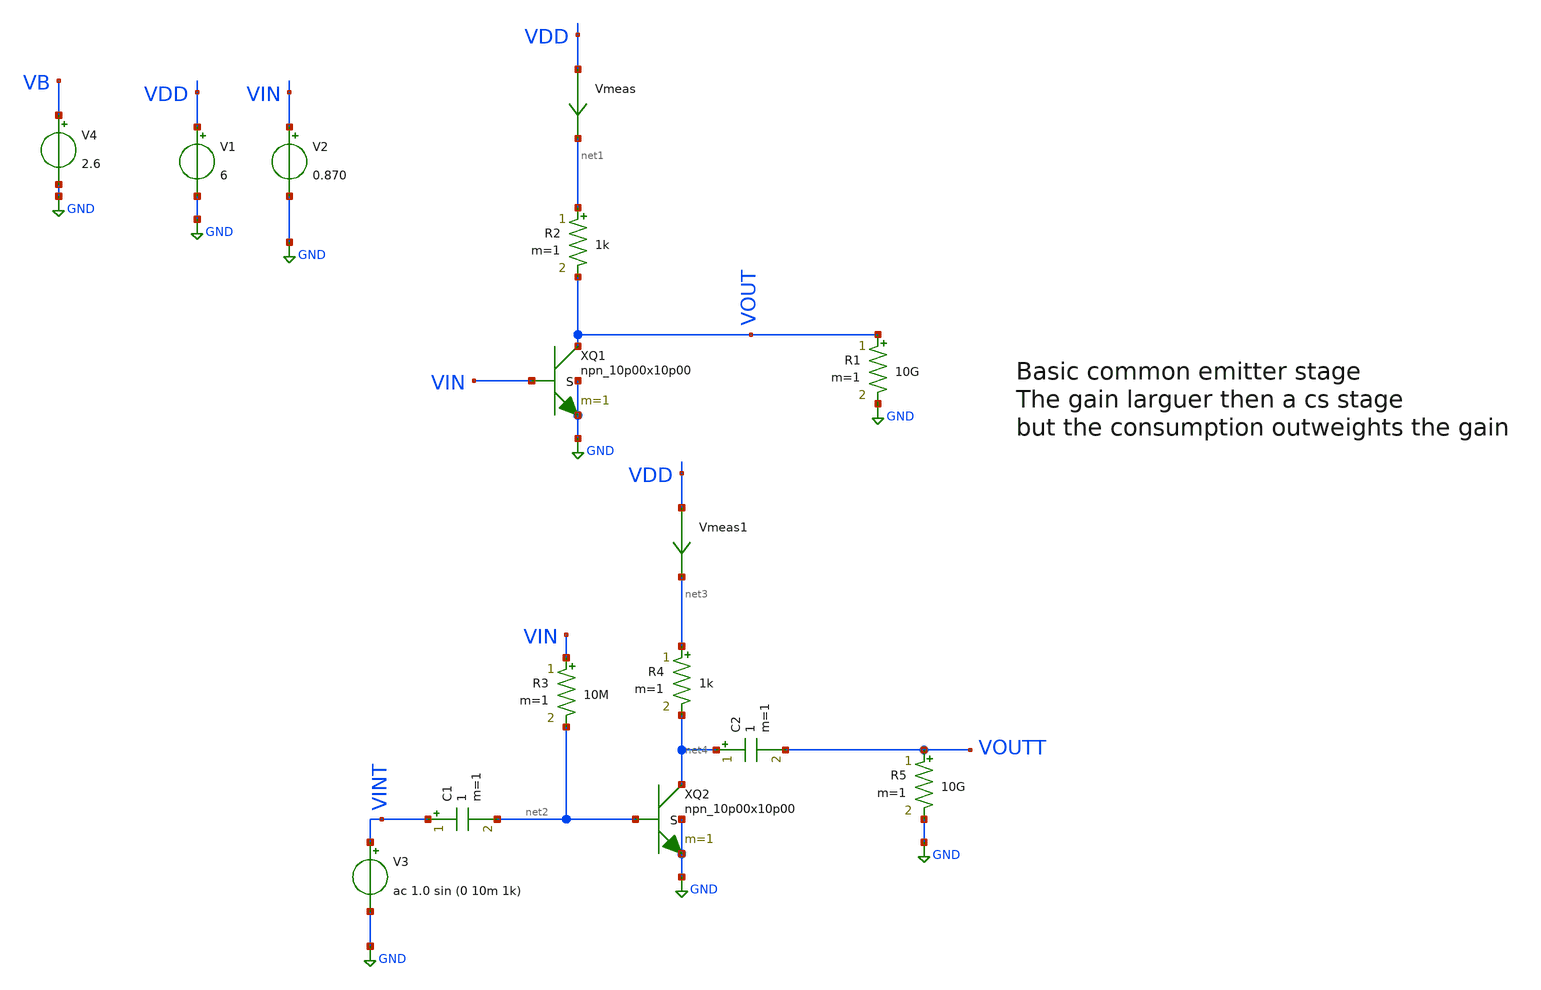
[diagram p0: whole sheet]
** sch_path: basic_circuits/bipolar_stage_1.sch
**.subckt bipolar_stage_1
Vmeas VDD net1 0
.save i(vmeas)
V1 VDD GND 6
V2 VIN GND 0.870
V3 VINT GND ac 1.0 sin (0 10m 1k)
R3 VIN net2 10M m=1
R5 VOUTT GND 10G m=1
V4 VB GND 2.6
R1 VOUT GND 10G m=1
C1 VINT net2 1 m=1
R2 net1 VOUT 1k m=1
XQ1 VOUT VIN GND GND npn_10p00x10p00 m=1
Vmeas1 VDD net3 0
.save i(vmeas1)
R4 net3 net4 1k m=1
XQ2 net4 net2 GND GND npn_10p00x10p00 m=1
C2 net4 VOUTT 1 m=1
**** begin user architecture code

**************************************************************
**************************************************************
**************************************************************
**************************************************************
**************************************************************
*LIBs*********************************************************
**************************************************************
**************************************************************
**************************************************************
**************************************************************
**************************************************************
.include $::180MCU_MODELS/design.ngspice
*.lib $::180MCU_MODELS/sm141064.ngspice statistical *use statistical if you want global and parameter mismatch
*.lib $::180MCU_MODELS/sm141064.ngspice res_statistical
.lib $::180MCU_MODELS/sm141064.ngspice typical
.lib $::180MCU_MODELS/sm141064.ngspice res_typical
.lib $::180MCU_MODELS/sm141064.ngspice moscap_typical
.lib $::180MCU_MODELS/sm141064.ngspice bjt_typical
.lib $::180MCU_MODELS/sm141064.ngspice diode_typical
.lib $::180MCU_MODELS/sm141064.ngspice mimcap_typical
**************************************************************
**************************************************************
**************************************************************
**************************************************************
**************************************************************
*Corners/montecarlo options***********************************
**************************************************************
**************************************************************
**************************************************************
**************************************************************
**************************************************************
.TEMP 27
.param   sw_stat_global = 1   sw_stat_mism = 1  mc_skew = 3  res_mc_skew = 3  cap_mc_skew = 3
+  fnoicor = 1
**************************************************************
**************************************************************
**************************************************************
**************************************************************
*SIMULATION and Plots*****************************************
**************************************************************
**************************************************************
**************************************************************
**************************************************************
.control
save all
dc V2 0 3.3 0.01
*dc simulation
plot v(VOUT) v(VIN) deriv(v(VOUT))
*ploting VIN VOUT and the voltage gain
plot i(Vmeas)
*ploting the current for curiosity
tran 100ns 2m
*transient simulation
plot (v(VINT)) (v(VOUTT))
*simple plot to exemplify the gain
fft v(VOUTT) v(VINT)
*fast fourier transfor
plot mag(v(VOUTT)) mag(v(VINT))
* analyse the frequency spectrum of the transient waves, to detect distortion
ac dec 20 1 50G
*simple ac simulation
plot v(VOUTT)
*gain in function of the input frequency
.endc

**** end user architecture code
**.ends
.GLOBAL GND
.end
